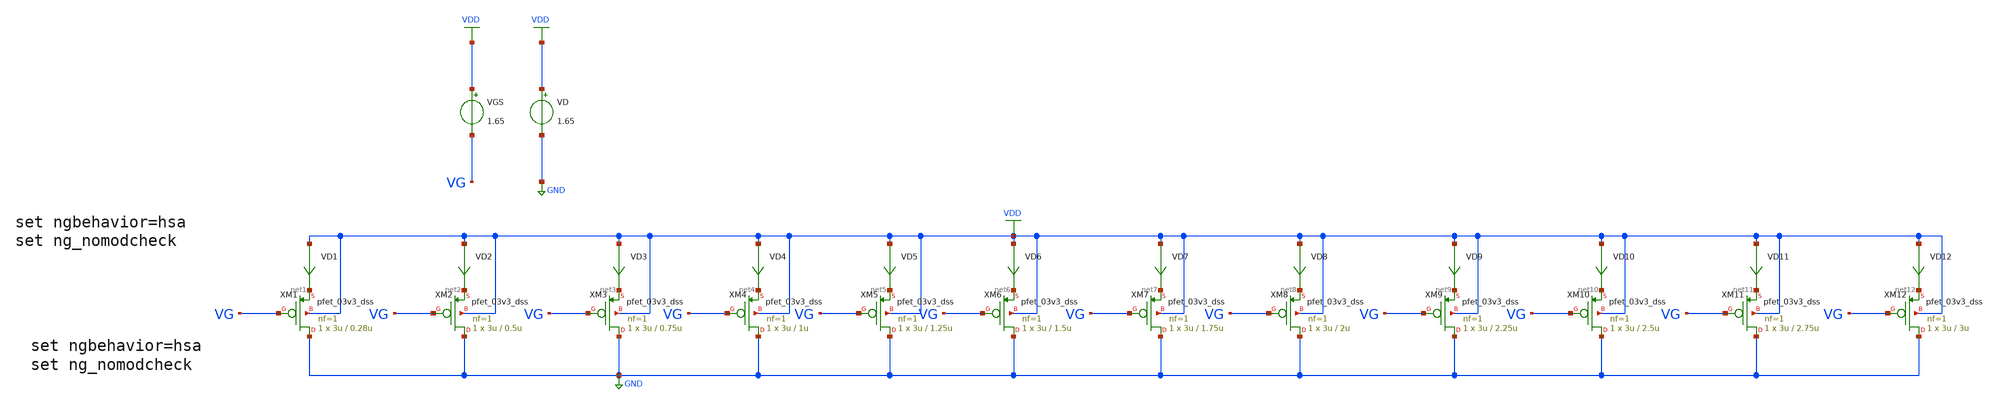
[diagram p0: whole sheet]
** sch_path: gmid Data/PMOS_03v3_DSS/PMOS_03v3_DSS/gmid_pmos_03v3_dss.sch
**.subckt gmid_pmos_03v3_dss
VGS VDD VG 1.65
VD VDD GND 1.65
VD1 VDD net1 0
.save i(vd1)
VD2 VDD net2 0
.save i(vd2)
VD3 VDD net3 0
.save i(vd3)
VD4 VDD net4 0
.save i(vd4)
VD5 VDD net5 0
.save i(vd5)
VD6 VDD net6 0
.save i(vd6)
VD7 VDD net7 0
.save i(vd7)
VD8 VDD net8 0
.save i(vd8)
VD9 VDD net9 0
.save i(vd9)
VD10 VDD net10 0
.save i(vd10)
VD11 VDD net11 0
.save i(vd11)
VD12 VDD net12 0
.save i(vd12)
XM1 GND VG net1 VDD pfet_03v3_dss L=0.28u W=3u nf=1 ad='int((nf+1)/2) * W/nf * 0.18u' as='int((nf+2)/2) * W/nf * 0.18u'
+ pd='2*int((nf+1)/2) * (W/nf + 0.18u)' ps='2*int((nf+2)/2) * (W/nf + 0.18u)' nrd='0.18u / W' nrs='0.18u / W'
+ sa=0 sb=0 sd=0 m=1
XM2 GND VG net2 VDD pfet_03v3_dss L=0.5u W=3u nf=1 ad='int((nf+1)/2) * W/nf * 0.18u' as='int((nf+2)/2) * W/nf * 0.18u'
+ pd='2*int((nf+1)/2) * (W/nf + 0.18u)' ps='2*int((nf+2)/2) * (W/nf + 0.18u)' nrd='0.18u / W' nrs='0.18u / W'
+ sa=0 sb=0 sd=0 m=1
XM3 GND VG net3 VDD pfet_03v3_dss L=0.75u W=3u nf=1 ad='int((nf+1)/2) * W/nf * 0.18u' as='int((nf+2)/2) * W/nf * 0.18u'
+ pd='2*int((nf+1)/2) * (W/nf + 0.18u)' ps='2*int((nf+2)/2) * (W/nf + 0.18u)' nrd='0.18u / W' nrs='0.18u / W'
+ sa=0 sb=0 sd=0 m=1
XM4 GND VG net4 VDD pfet_03v3_dss L=1u W=3u nf=1 ad='int((nf+1)/2) * W/nf * 0.18u' as='int((nf+2)/2) * W/nf * 0.18u'
+ pd='2*int((nf+1)/2) * (W/nf + 0.18u)' ps='2*int((nf+2)/2) * (W/nf + 0.18u)' nrd='0.18u / W' nrs='0.18u / W'
+ sa=0 sb=0 sd=0 m=1
XM5 GND VG net5 VDD pfet_03v3_dss L=1.25u W=3u nf=1 ad='int((nf+1)/2) * W/nf * 0.18u' as='int((nf+2)/2) * W/nf * 0.18u'
+ pd='2*int((nf+1)/2) * (W/nf + 0.18u)' ps='2*int((nf+2)/2) * (W/nf + 0.18u)' nrd='0.18u / W' nrs='0.18u / W'
+ sa=0 sb=0 sd=0 m=1
XM6 GND VG net6 VDD pfet_03v3_dss L=1.5u W=3u nf=1 ad='int((nf+1)/2) * W/nf * 0.18u' as='int((nf+2)/2) * W/nf * 0.18u'
+ pd='2*int((nf+1)/2) * (W/nf + 0.18u)' ps='2*int((nf+2)/2) * (W/nf + 0.18u)' nrd='0.18u / W' nrs='0.18u / W'
+ sa=0 sb=0 sd=0 m=1
XM7 GND VG net7 VDD pfet_03v3_dss L=1.75u W=3u nf=1 ad='int((nf+1)/2) * W/nf * 0.18u' as='int((nf+2)/2) * W/nf * 0.18u'
+ pd='2*int((nf+1)/2) * (W/nf + 0.18u)' ps='2*int((nf+2)/2) * (W/nf + 0.18u)' nrd='0.18u / W' nrs='0.18u / W'
+ sa=0 sb=0 sd=0 m=1
XM8 GND VG net8 VDD pfet_03v3_dss L=2u W=3u nf=1 ad='int((nf+1)/2) * W/nf * 0.18u' as='int((nf+2)/2) * W/nf * 0.18u'
+ pd='2*int((nf+1)/2) * (W/nf + 0.18u)' ps='2*int((nf+2)/2) * (W/nf + 0.18u)' nrd='0.18u / W' nrs='0.18u / W'
+ sa=0 sb=0 sd=0 m=1
XM9 GND VG net9 VDD pfet_03v3_dss L=2.25u W=3u nf=1 ad='int((nf+1)/2) * W/nf * 0.18u' as='int((nf+2)/2) * W/nf * 0.18u'
+ pd='2*int((nf+1)/2) * (W/nf + 0.18u)' ps='2*int((nf+2)/2) * (W/nf + 0.18u)' nrd='0.18u / W' nrs='0.18u / W'
+ sa=0 sb=0 sd=0 m=1
XM10 GND VG net10 VDD pfet_03v3_dss L=2.5u W=3u nf=1 ad='int((nf+1)/2) * W/nf * 0.18u' as='int((nf+2)/2) * W/nf * 0.18u'
+ pd='2*int((nf+1)/2) * (W/nf + 0.18u)' ps='2*int((nf+2)/2) * (W/nf + 0.18u)' nrd='0.18u / W' nrs='0.18u / W'
+ sa=0 sb=0 sd=0 m=1
XM11 GND VG net11 VDD pfet_03v3_dss L=2.75u W=3u nf=1 ad='int((nf+1)/2) * W/nf * 0.18u' as='int((nf+2)/2) * W/nf * 0.18u'
+ pd='2*int((nf+1)/2) * (W/nf + 0.18u)' ps='2*int((nf+2)/2) * (W/nf + 0.18u)' nrd='0.18u / W' nrs='0.18u / W'
+ sa=0 sb=0 sd=0 m=1
XM12 GND VG net12 VDD pfet_03v3_dss L=3u W=3u nf=1 ad='int((nf+1)/2) * W/nf * 0.18u' as='int((nf+2)/2) * W/nf * 0.18u'
+ pd='2*int((nf+1)/2) * (W/nf + 0.18u)' ps='2*int((nf+2)/2) * (W/nf + 0.18u)' nrd='0.18u / W' nrs='0.18u / W'
+ sa=0 sb=0 sd=0 m=1
**** begin user architecture code


.save @m.xm1.m0[gm]
.save @m.xm1.m0[vth]
.save @m.xm1.m0[gds]
.save @m.xm1.m0[cgg]
.save @m.xm1.m0[cgs]
.save @m.xm1.m0[cgd]
.save @m.xm2.m0[gm]
.save @m.xm2.m0[vth]
.save @m.xm2.m0[gds]
.save @m.xm2.m0[cgg]
.save @m.xm2.m0[cgs]
.save @m.xm2.m0[cgd]
.save @m.xm3.m0[gm]
.save @m.xm3.m0[vth]
.save @m.xm3.m0[gds]
.save @m.xm3.m0[cgg]
.save @m.xm3.m0[cgs]
.save @m.xm3.m0[cgd]
.save @m.xm4.m0[gm]
.save @m.xm4.m0[vth]
.save @m.xm4.m0[gds]
.save @m.xm4.m0[cgg]
.save @m.xm4.m0[cgs]
.save @m.xm4.m0[cgd]
.save @m.xm5.m0[gm]
.save @m.xm5.m0[vth]
.save @m.xm5.m0[gds]
.save @m.xm5.m0[cgg]
.save @m.xm5.m0[cgs]
.save @m.xm5.m0[cgd]
.save @m.xm6.m0[gm]
.save @m.xm6.m0[vth]
.save @m.xm6.m0[gds]
.save @m.xm6.m0[cgg]
.save @m.xm6.m0[cgs]
.save @m.xm6.m0[cgd]
.save @m.xm7.m0[gm]
.save @m.xm7.m0[vth]
.save @m.xm7.m0[gds]
.save @m.xm7.m0[cgg]
.save @m.xm7.m0[cgs]
.save @m.xm7.m0[cgd]
.save @m.xm8.m0[gm]
.save @m.xm8.m0[vth]
.save @m.xm8.m0[gds]
.save @m.xm8.m0[cgg]
.save @m.xm8.m0[cgs]
.save @m.xm8.m0[cgd]
.save @m.xm9.m0[gm]
.save @m.xm9.m0[vth]
.save @m.xm9.m0[gds]
.save @m.xm9.m0[cgg]
.save @m.xm9.m0[cgs]
.save @m.xm9.m0[cgd]
.save @m.xm10.m0[gm]
.save @m.xm10.m0[vth]
.save @m.xm10.m0[gds]
.save @m.xm10.m0[cgg]
.save @m.xm10.m0[cgs]
.save @m.xm10.m0[cgd]
.save @m.xm11.m0[gm]
.save @m.xm11.m0[vth]
.save @m.xm11.m0[gds]
.save @m.xm11.m0[cgg]
.save @m.xm11.m0[cgs]
.save @m.xm11.m0[cgd]
.save @m.xm12.m0[gm]
.save @m.xm12.m0[vth]
.save @m.xm12.m0[gds]
.save @m.xm12.m0[cgg]
.save @m.xm12.m0[cgs]
.save @m.xm12.m0[cgd]




.lib /foss/pdks/volare/gf180mcu/versions/0fe599b2afb6708d281543108caf8310912f54af/gf180mcuD/libs.tech/ngspice/sm141064.ngspice typical
.include /foss/pdks/volare/gf180mcu/versions/0fe599b2afb6708d281543108caf8310912f54af/gf180mcuD/libs.tech/ngspice/design.ngspice

*.include $::180MCU_MODELS/design.ngspice
*.lib $::180MCU_MODELS/sm141064.ngspice typical




* ngspice commands
.option wnflag=1
.option .savecurrents
.control
save all
dc VGS 0.05 3 0.1m
** remove zero length vectors to prevent write errors
remzerovec
write /foss/designs/PDK-CHAR/GF180-MCUD/PMOS_03v3_DSS/gmid_PMOS_03v3_DSS_tb.raw

plot @m.xm1.m0[gm]
plot @m.xm2.m0[gm]
plot @m.xm3.m0[gm]
plot @m.xm4.m0[gm]
plot @m.xm5.m0[gm]
plot @m.xm6.m0[gm]
plot @m.xm7.m0[gm]
plot @m.xm8.m0[gm]
plot @m.xm9.m0[gm]
plot @m.xm10.m0[gm]
plot @m.xm11.m0[gm]
plot @m.xm12.m0[gm]

wrdata /foss/designs/PDK-CHAR/GF180-MCUD/PMOS_03v3_DSS/gmid_pmos_1_pfet_03v3_dss_tb.txt
+ @m.xm1.m0[gm] i(VD1) @m.xm1.m0[vth] @m.xm1.m0[gds] @m.xm1.m0[cgg] @m.xm1.m0[cgs] @m.xm1.m0[cgd]
wrdata /foss/designs/PDK-CHAR/GF180-MCUD/PMOS_03v3_DSS/gmid_pmos_2_pfet_03v3_dss_tb.txt
+ @m.xm2.m0[gm] i(VD2) @m.xm2.m0[vth] @m.xm2.m0[gds] @m.xm2.m0[cgg] @m.xm2.m0[cgs] @m.xm2.m0[cgd]
wrdata /foss/designs/PDK-CHAR/GF180-MCUD/PMOS_03v3_DSS/gmid_pmos_3_pfet_03v3_dss_tb.txt
+ @m.xm3.m0[gm] i(VD3) @m.xm3.m0[vth] @m.xm3.m0[gds] @m.xm3.m0[cgg] @m.xm3.m0[cgs] @m.xm3.m0[cgd]
wrdata /foss/designs/PDK-CHAR/GF180-MCUD/PMOS_03v3_DSS/gmid_pmos_4_pfet_03v3_dss_tb.txt
+ @m.xm4.m0[gm] i(VD4) @m.xm4.m0[vth] @m.xm4.m0[gds] @m.xm4.m0[cgg] @m.xm4.m0[cgs] @m.xm4.m0[cgd]
wrdata /foss/designs/PDK-CHAR/GF180-MCUD/PMOS_03v3_DSS/gmid_pmos_5_pfet_03v3_dss_tb.txt
+ @m.xm5.m0[gm] i(VD5) @m.xm5.m0[vth] @m.xm5.m0[gds] @m.xm5.m0[cgg] @m.xm5.m0[cgs] @m.xm5.m0[cgd]
wrdata /foss/designs/PDK-CHAR/GF180-MCUD/PMOS_03v3_DSS/gmid_pmos_6_pfet_03v3_dss_tb.txt
+ @m.xm6.m0[gm] i(VD6) @m.xm6.m0[vth] @m.xm6.m0[gds] @m.xm6.m0[cgg] @m.xm6.m0[cgs] @m.xm6.m0[cgd]
wrdata /foss/designs/PDK-CHAR/GF180-MCUD/PMOS_03v3_DSS/gmid_pmos_7_pfet_03v3_dss_tb.txt
+ @m.xm7.m0[gm] i(VD7) @m.xm7.m0[vth] @m.xm7.m0[gds] @m.xm7.m0[cgg] @m.xm7.m0[cgs] @m.xm7.m0[cgd]
wrdata /foss/designs/PDK-CHAR/GF180-MCUD/PMOS_03v3_DSS/gmid_pmos_8_pfet_03v3_dss_tb.txt
+ @m.xm8.m0[gm] i(VD8) @m.xm8.m0[vth] @m.xm8.m0[gds] @m.xm8.m0[cgg] @m.xm8.m0[cgs] @m.xm8.m0[cgd]
wrdata /foss/designs/PDK-CHAR/GF180-MCUD/PMOS_03v3_DSS/gmid_pmos_9_pfet_03v3_dss_tb.txt
+ @m.xm9.m0[gm] i(VD9) @m.xm9.m0[vth] @m.xm9.m0[gds] @m.xm9.m0[cgg] @m.xm9.m0[cgs] @m.xm9.m0[cgd]
wrdata /foss/designs/PDK-CHAR/GF180-MCUD/PMOS_03v3_DSS/gmid_pmos_10_pfet_03v3_dss_tb.txt
+ @m.xm10.m0[gm] i(VD10) @m.xm10.m0[vth] @m.xm10.m0[gds] @m.xm10.m0[cgg] @m.xm10.m0[cgs] @m.xm10.m0[cgd]
wrdata /foss/designs/PDK-CHAR/GF180-MCUD/PMOS_03v3_DSS/gmid_pmos_11_pfet_03v3_dss_tb.txt
+ @m.xm11.m0[gm] i(VD11) @m.xm11.m0[vth] @m.xm11.m0[gds] @m.xm11.m0[cgg] @m.xm11.m0[cgs] @m.xm11.m0[cgd]
wrdata /foss/designs/PDK-CHAR/GF180-MCUD/PMOS_03v3_DSS/gmid_pmos_12_pfet_03v3_dss_tb.txt
+ @m.xm12.m0[gm] i(VD12) @m.xm12.m0[vth] @m.xm12.m0[gds] @m.xm12.m0[cgg] @m.xm12.m0[cgs] @m.xm12.m0[cgd]
set appendwrite
op
remzerovec
write /foss/designs/PDK-CHAR/GF180-MCUD/PMOS_03v3_DSS/gmid_PMOS_03v3_DSS_tb.raw
**quit 0
.endc


**** end user architecture code
**.ends
.GLOBAL GND
.GLOBAL VDD
.end
